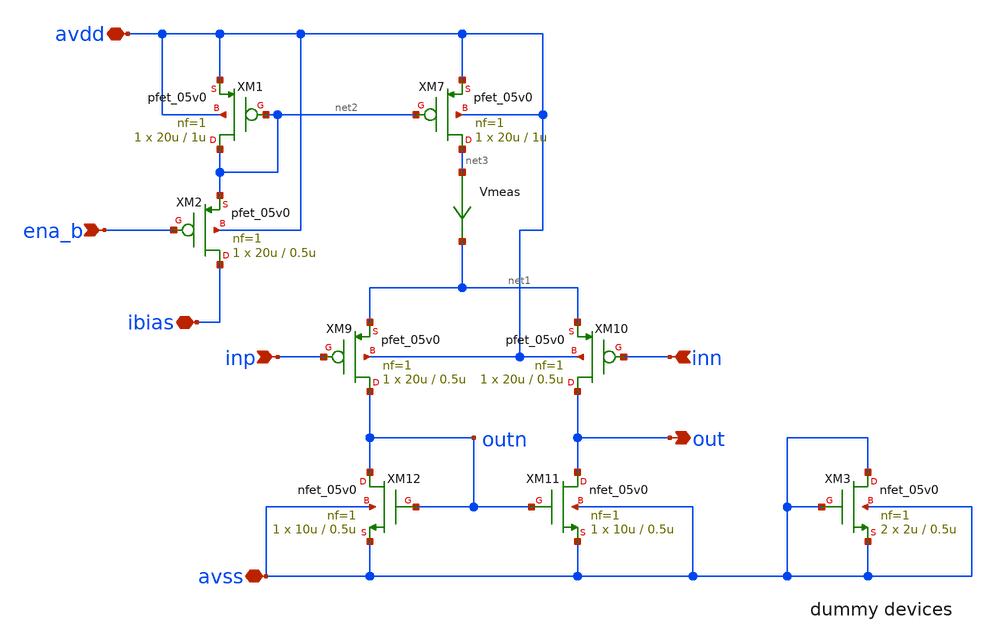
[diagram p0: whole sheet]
** sch_path: xschem/p_amp_large.sch
**.subckt p_amp_large avdd avss ena_b inp inn out ibias
*.iopin avdd
*.iopin avss
*.ipin ena_b
*.ipin inp
*.ipin inn
*.opin out
*.iopin ibias
XM7 net3 net2 avdd avdd pfet_05v0 L=1u W=20u nf=1 ad='int((nf+1)/2) * W/nf * 0.18u' as='int((nf+2)/2) * W/nf * 0.18u'
+ pd='2*int((nf+1)/2) * (W/nf + 0.18u)' ps='2*int((nf+2)/2) * (W/nf + 0.18u)' nrd='0.18u / W' nrs='0.18u / W'
+ sa=0 sb=0 sd=0 m=1 par=1
XM9 outn inp net1 avdd pfet_05v0 L=0.5u W=20u nf=1 ad='int((nf+1)/2) * W/nf * 0.18u' as='int((nf+2)/2) * W/nf * 0.18u'
+ pd='2*int((nf+1)/2) * (W/nf + 0.18u)' ps='2*int((nf+2)/2) * (W/nf + 0.18u)' nrd='0.18u / W' nrs='0.18u / W'
+ sa=0 sb=0 sd=0 m=1 par=1
XM10 out inn net1 avdd pfet_05v0 L=0.5u W=20u nf=1 ad='int((nf+1)/2) * W/nf * 0.18u' as='int((nf+2)/2) * W/nf * 0.18u'
+ pd='2*int((nf+1)/2) * (W/nf + 0.18u)' ps='2*int((nf+2)/2) * (W/nf + 0.18u)' nrd='0.18u / W' nrs='0.18u / W'
+ sa=0 sb=0 sd=0 m=1 par=1
XM11 out outn avss avss nfet_05v0 L=0.5u W=10u nf=1 ad='int((nf+1)/2) * W/nf * 0.18u' as='int((nf+2)/2) * W/nf * 0.18u'
+ pd='2*int((nf+1)/2) * (W/nf + 0.18u)' ps='2*int((nf+2)/2) * (W/nf + 0.18u)' nrd='0.18u / W' nrs='0.18u / W'
+ sa=0 sb=0 sd=0 m=1
XM12 outn outn avss avss nfet_05v0 L=0.5u W=10u nf=1 ad='int((nf+1)/2) * W/nf * 0.18u' as='int((nf+2)/2) * W/nf * 0.18u'
+ pd='2*int((nf+1)/2) * (W/nf + 0.18u)' ps='2*int((nf+2)/2) * (W/nf + 0.18u)' nrd='0.18u / W' nrs='0.18u / W'
+ sa=0 sb=0 sd=0 m=1
XM1 net2 net2 avdd avdd pfet_05v0 L=1u W=20u nf=1 ad='int((nf+1)/2) * W/nf * 0.18u' as='int((nf+2)/2) * W/nf * 0.18u'
+ pd='2*int((nf+1)/2) * (W/nf + 0.18u)' ps='2*int((nf+2)/2) * (W/nf + 0.18u)' nrd='0.18u / W' nrs='0.18u / W'
+ sa=0 sb=0 sd=0 m=1 par=1
XM2 ibias ena_b net2 avdd pfet_05v0 L=0.5u W=20u nf=1 ad='int((nf+1)/2) * W/nf * 0.18u' as='int((nf+2)/2) * W/nf * 0.18u'
+ pd='2*int((nf+1)/2) * (W/nf + 0.18u)' ps='2*int((nf+2)/2) * (W/nf + 0.18u)' nrd='0.18u / W' nrs='0.18u / W'
+ sa=0 sb=0 sd=0 m=1 par=1
Vmeas net3 net1 0
.save i(vmeas)
XM3 avss avss avss avss nfet_05v0 L=0.5u W=2u nf=1 ad='int((nf+1)/2) * W/nf * 0.18u' as='int((nf+2)/2) * W/nf * 0.18u'
+ pd='2*int((nf+1)/2) * (W/nf + 0.18u)' ps='2*int((nf+2)/2) * (W/nf + 0.18u)' nrd='0.18u / W' nrs='0.18u / W'
+ sa=0 sb=0 sd=0 m=2
**.ends
.end
